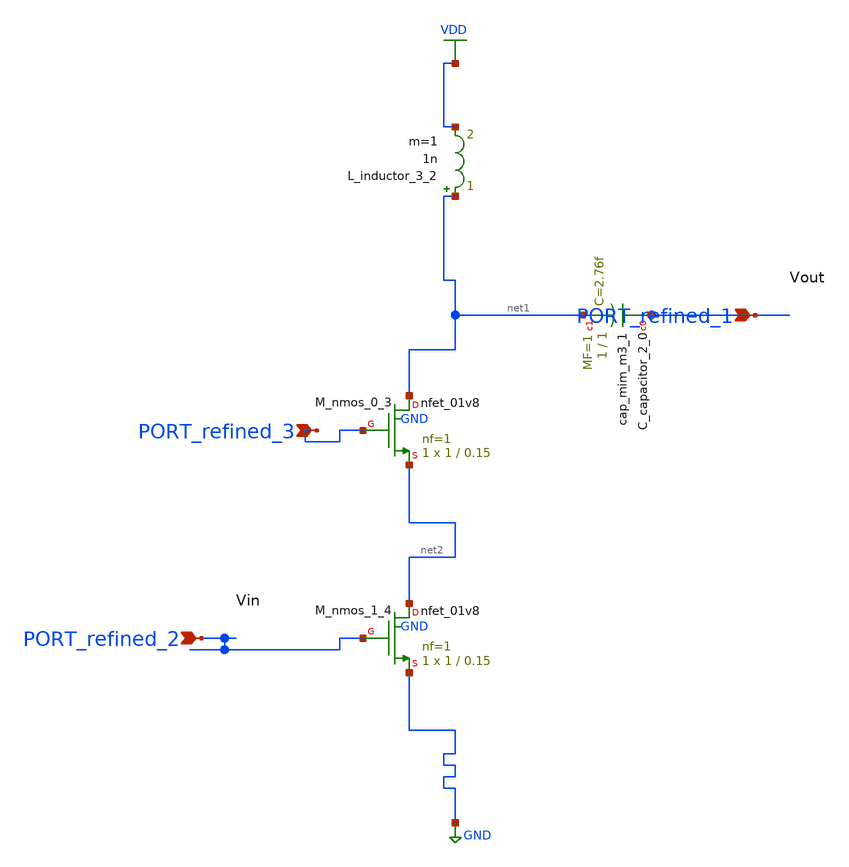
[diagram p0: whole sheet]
** sch_path: schematics/SchemGen/no_doi_42_001.sch
**.subckt no_doi_42_001 PORT_refined_3 PORT_refined_2 PORT_refined_1
*.ipin PORT_refined_3
*.ipin PORT_refined_2
*.ipin PORT_refined_1
XC_capacitor_2_0 PORT_refined_1 net1 sky130_fd_pr__cap_mim_m3_1 W=1 L=1 MF=1 m=1
L_inductor_3_2 net1 VDD 1n m=1
XM_nmos_0_3 net1 PORT_refined_3 net2 GND sky130_fd_pr__nfet_01v8 L=0.15 W=1 nf=1 ad='int((1 + 1)/2) * 1 / 1 * 0.29'
+ as='int((1 + 2)/2) * 1 / 1 * 0.29' pd='2*int((1 + 1)/2) * (1 / 1 + 0.29)' ps='2*int((1 + 2)/2) * (1 / 1 + 0.29)'
+ nrd='0.29 / 1 ' nrs='0.29 / 1 ' sa=0 sb=0 sd=0 mult=1 m=1
XM_nmos_1_4 net2 PORT_refined_2 GND GND sky130_fd_pr__nfet_01v8 L=0.15 W=1 nf=1 ad='int((1 + 1)/2) * 1 / 1 * 0.29'
+ as='int((1 + 2)/2) * 1 / 1 * 0.29' pd='2*int((1 + 1)/2) * (1 / 1 + 0.29)' ps='2*int((1 + 2)/2) * (1 / 1 + 0.29)'
+ nrd='0.29 / 1 ' nrs='0.29 / 1 ' sa=0 sb=0 sd=0 mult=1 m=1
**.ends
.GLOBAL GND
.GLOBAL VDD
.end
